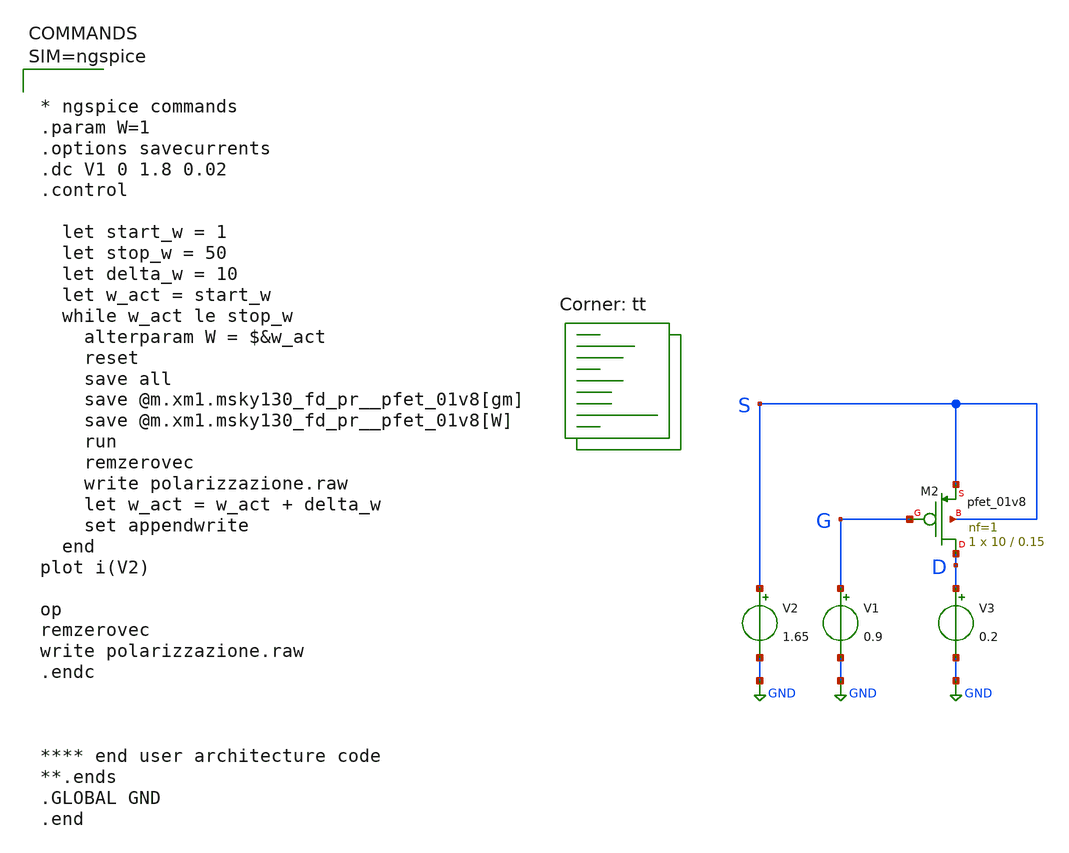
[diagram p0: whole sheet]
** sch_path: xschem/polarizzazione.sch
**.subckt polarizzazione
XM2 D G S S sky130_fd_pr__pfet_01v8 L=0.15 W=10 nf=1 ad='int((nf+1)/2) * W/nf * 0.29' as='int((nf+2)/2) * W/nf * 0.29'
+ pd='2*int((nf+1)/2) * (W/nf + 0.29)' ps='2*int((nf+2)/2) * (W/nf + 0.29)' nrd='0.29 / W' nrs='0.29 / W'
+ sa=0 sb=0 sd=0 mult=1 m=1
V1 G GND 0.9
V2 S GND 1.65
V3 D GND 0.2
**** begin user architecture code
.lib $::SKYWATER_MODELS/sky130.lib.spice tt



* ngspice commands
.param W=1
.options savecurrents
.dc V1 0 1.8 0.02
.control

  let start_w = 1
  let stop_w = 50
  let delta_w = 10
  let w_act = start_w
  while w_act le stop_w
    alterparam W = $&w_act
    reset
    save all
    save @m.xm1.msky130_fd_pr__pfet_01v8[gm]
    save @m.xm1.msky130_fd_pr__pfet_01v8[W]
    run
    remzerovec
    write polarizzazione.raw
    let w_act = w_act + delta_w
    set appendwrite
  end
plot i(V2)

op
remzerovec
write polarizzazione.raw
.endc



**** end user architecture code
**.ends
.GLOBAL GND
.end



**** end user architecture code
**.ends
.GLOBAL GND
.end
